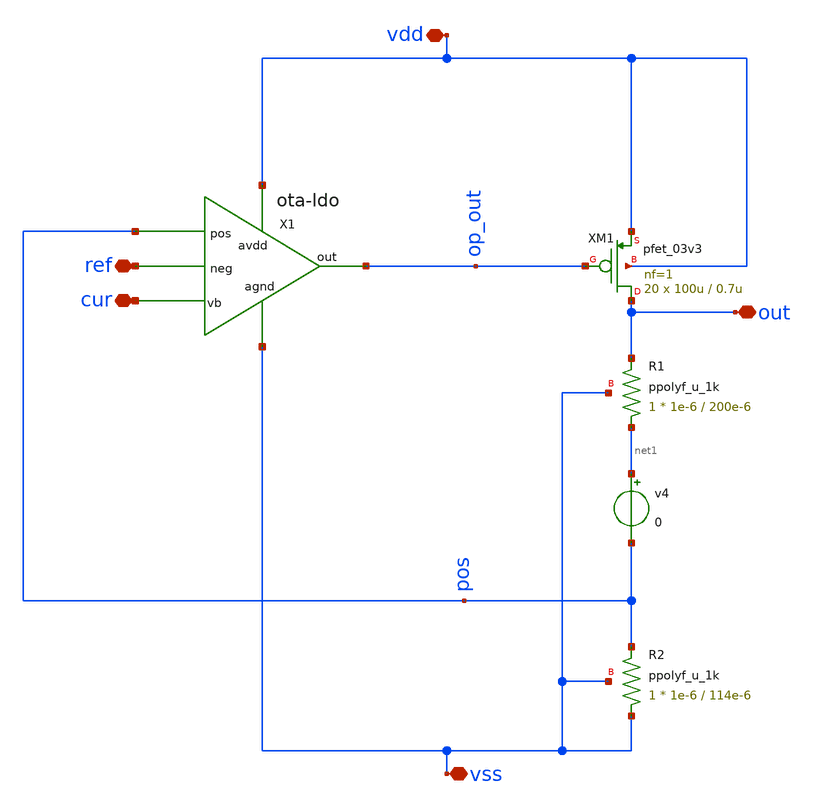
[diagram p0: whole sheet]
** sch_path: LDO/xschem/ldo/ldo.sch

.include $env(PDK_ROOT)/$env(PDK)/libs.tech/ngspice/design.ngspice
.lib $env(PDK_ROOT)/$env(PDK)/libs.tech/ngspice/sm141064.ngspice typical
.lib $env(PDK_ROOT)/$env(PDK)/libs.tech/ngspice/sm141064.ngspice mimcap_statistical
.lib $env(PDK_ROOT)/$env(PDK)/libs.tech/ngspice/sm141064.ngspice cap_mim
.lib $env(PDK_ROOT)/$env(PDK)/libs.tech/ngspice/sm141064.ngspice res_typical

**.subckt ldo ref out cur vss vdd
*.iopin ref
*.iopin out
*.iopin cur
*.iopin vss
*.iopin vdd
X1 vdd op_out ref pos cur vss ota-ldo
XM1 out op_out vdd vdd pfet_03v3 L=0.7u W=100u nf=1 ad='int((nf+1)/2) * W/nf * 0.18u' as='int((nf+2)/2) * W/nf * 0.18u'
+ pd='2*int((nf+1)/2) * (W/nf + 0.18u)' ps='2*int((nf+2)/2) * (W/nf + 0.18u)' nrd='0.18u / W' nrs='0.18u / W'
+ sa=0 sb=0 sd=0 m=20
XR1 net1 out vss ppolyf_u_1k r_width=1e-6 r_length=200e-6 m=1
XR2 vss pos vss ppolyf_u_1k r_width=1e-6 r_length=114e-6 m=1
v4 net1 pos 0
**.ends

* expanding   symbol:  ../ota-ldo/ota-ldo.sym # of pins=6
** sym_path: LDO/xschem/ota-ldo/ota-ldo.sym
** sch_path: LDO/xschem/ota-ldo/ota-ldo.sch
.subckt ota-ldo avdd out neg pos vb agnd
*.iopin vb
*.iopin avdd
*.iopin agnd
*.ipin neg
*.ipin pos
*.opin out
XC2 net2 out cap_mim_1f5fF c_width=50e-6 c_length=20e-6 m=1
XM1 net1 neg net3 agnd nfet_03v3 L=0.3u W=10u nf=1 ad='int((nf+1)/2) * W/nf * 0.18u' as='int((nf+2)/2) * W/nf * 0.18u'
+ pd='2*int((nf+1)/2) * (W/nf + 0.18u)' ps='2*int((nf+2)/2) * (W/nf + 0.18u)' nrd='0.18u / W' nrs='0.18u / W'
+ sa=0 sb=0 sd=0 m=1
XM3 net1 net1 avdd avdd pfet_03v3 L=0.8u W=9u nf=1 ad='int((nf+1)/2) * W/nf * 0.18u' as='int((nf+2)/2) * W/nf * 0.18u'
+ pd='2*int((nf+1)/2) * (W/nf + 0.18u)' ps='2*int((nf+2)/2) * (W/nf + 0.18u)' nrd='0.18u / W' nrs='0.18u / W'
+ sa=0 sb=0 sd=0 m=1
XM2 net2 pos net3 agnd nfet_03v3 L=0.3u W=10u nf=1 ad='int((nf+1)/2) * W/nf * 0.18u' as='int((nf+2)/2) * W/nf * 0.18u'
+ pd='2*int((nf+1)/2) * (W/nf + 0.18u)' ps='2*int((nf+2)/2) * (W/nf + 0.18u)' nrd='0.18u / W' nrs='0.18u / W'
+ sa=0 sb=0 sd=0 m=1
XM4 net2 net1 avdd avdd pfet_03v3 L=0.8u W=9u nf=1 ad='int((nf+1)/2) * W/nf * 0.18u' as='int((nf+2)/2) * W/nf * 0.18u'
+ pd='2*int((nf+1)/2) * (W/nf + 0.18u)' ps='2*int((nf+2)/2) * (W/nf + 0.18u)' nrd='0.18u / W' nrs='0.18u / W'
+ sa=0 sb=0 sd=0 m=1
XM7 net3 vb agnd agnd nfet_03v3 L=0.8u W=16u nf=1 ad='int((nf+1)/2) * W/nf * 0.18u' as='int((nf+2)/2) * W/nf * 0.18u'
+ pd='2*int((nf+1)/2) * (W/nf + 0.18u)' ps='2*int((nf+2)/2) * (W/nf + 0.18u)' nrd='0.18u / W' nrs='0.18u / W'
+ sa=0 sb=0 sd=0 m=1
XM8 vb vb agnd agnd nfet_03v3 L=0.8u W=1.66u nf=1 ad='int((nf+1)/2) * W/nf * 0.18u' as='int((nf+2)/2) * W/nf * 0.18u'
+ pd='2*int((nf+1)/2) * (W/nf + 0.18u)' ps='2*int((nf+2)/2) * (W/nf + 0.18u)' nrd='0.18u / W' nrs='0.18u / W'
+ sa=0 sb=0 sd=0 m=1
XM5 out net2 avdd avdd pfet_03v3 L=0.4u W=60u nf=1 ad='int((nf+1)/2) * W/nf * 0.18u' as='int((nf+2)/2) * W/nf * 0.18u'
+ pd='2*int((nf+1)/2) * (W/nf + 0.18u)' ps='2*int((nf+2)/2) * (W/nf + 0.18u)' nrd='0.18u / W' nrs='0.18u / W'
+ sa=0 sb=0 sd=0 m=1
XM6 out vb agnd agnd nfet_03v3 L=0.8u W=60u nf=1 ad='int((nf+1)/2) * W/nf * 0.18u' as='int((nf+2)/2) * W/nf * 0.18u'
+ pd='2*int((nf+1)/2) * (W/nf + 0.18u)' ps='2*int((nf+2)/2) * (W/nf + 0.18u)' nrd='0.18u / W' nrs='0.18u / W'
+ sa=0 sb=0 sd=0 m=1
.ends

.end
